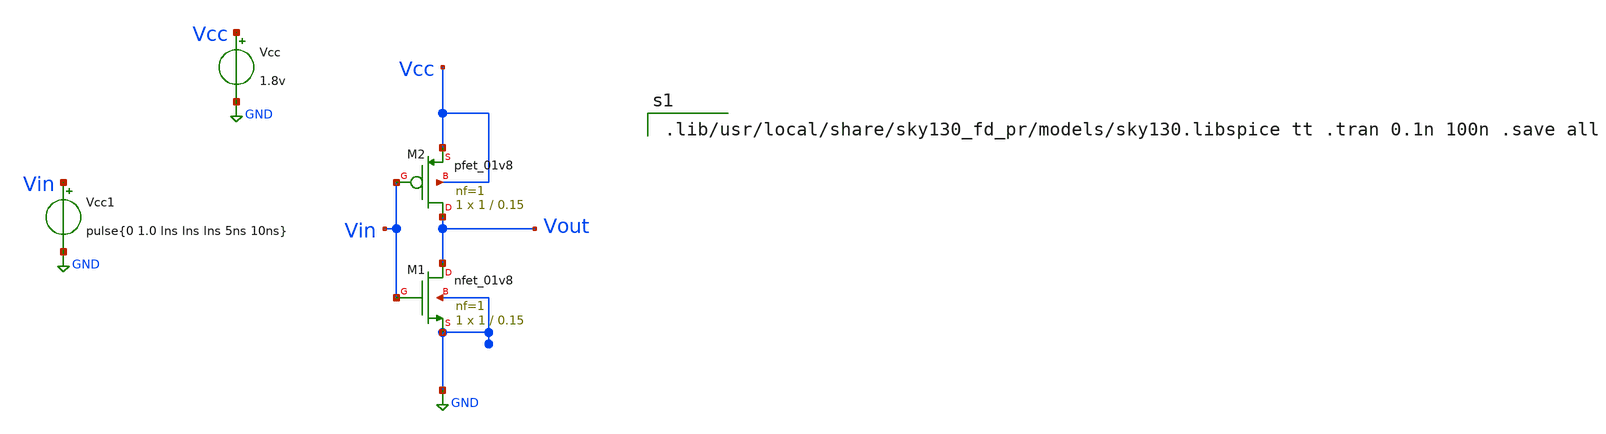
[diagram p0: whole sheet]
** sch_path: Xschem-Files/untitled.sch
**.subckt untitled
Vcc Vcc GND 1.8v
Vcc1 Vin GND pulse{0 1.0 lns lns lns 5ns 10ns}
XM1 Vout Vin GND GND sky130_fd_pr__nfet_01v8 L=0.15 W=1 nf=1 ad='int((1 + 1)/2) * 1 / 1 * 0.29' as='int((1 + 2)/2) * 1 / 1 * 0.29'
+ pd='2*int((1 + 1)/2) * (1 / 1 + 0.29)' ps='2*int((1 + 2)/2) * (1 / 1 + 0.29)' nrd='0.29 / 1 ' nrs='0.29 / 1 '
+ sa=0 sb=0 sd=0 mult=1 m=1
XM2 Vout Vin Vcc Vcc sky130_fd_pr__pfet_01v8 L=0.15 W=1 nf=1 ad='int((1 + 1)/2) * 1 / 1 * 0.29' as='int((1 + 2)/2) * 1 / 1 * 0.29'
+ pd='2*int((1 + 1)/2) * (1 / 1 + 0.29)' ps='2*int((1 + 2)/2) * (1 / 1 + 0.29)' nrd='0.29 / 1 ' nrs='0.29 / 1 '
+ sa=0 sb=0 sd=0 mult=1 m=1
**** begin user architecture code

.lib/usr/local/share/sky130_fd_pr/models/sky130.libspice tt .tran 0.1n 100n .save all

**** end user architecture code
**.ends
.GLOBAL GND
.end
